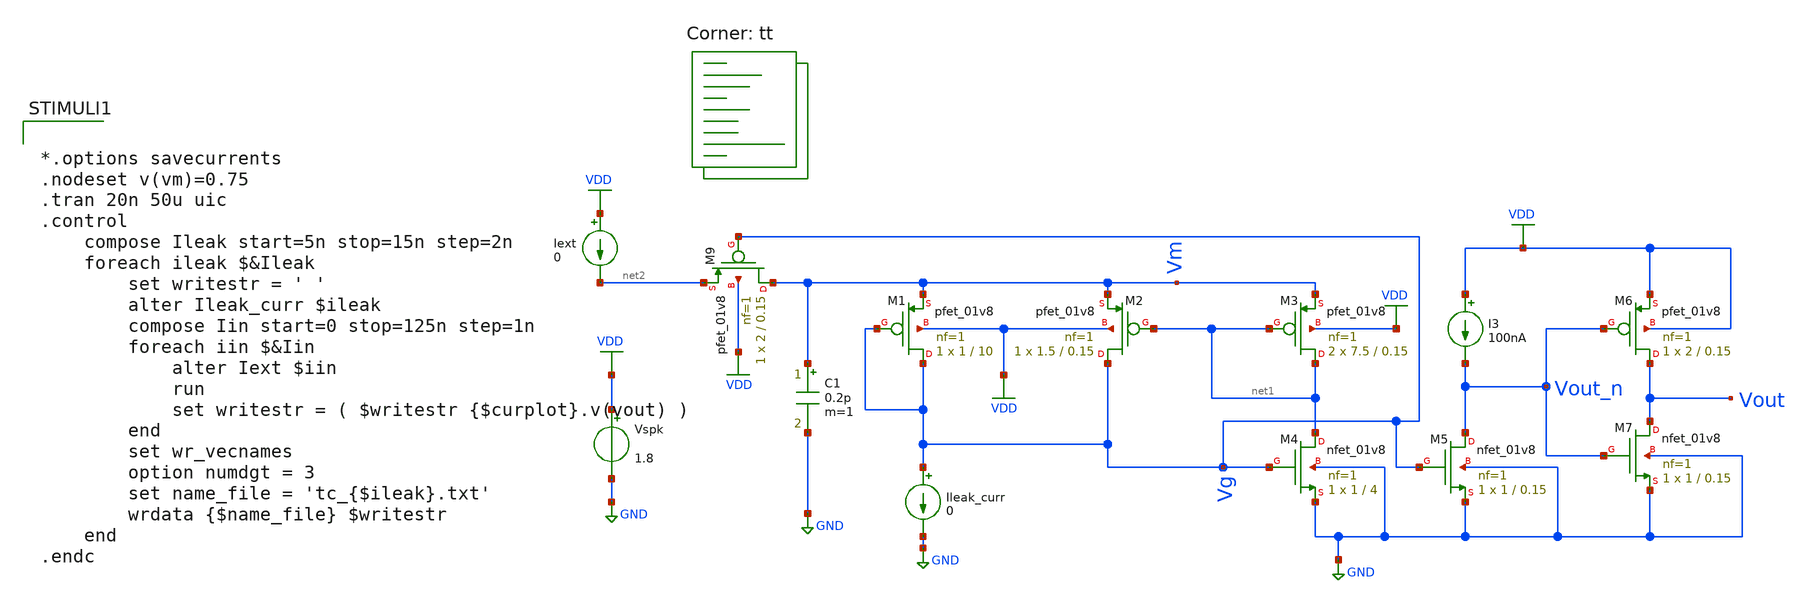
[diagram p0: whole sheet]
** sch_path: Neuron/ultralif/tb_tc_full.sch
**.subckt tb_tc_full
XM1 Vg Vg Vm VDD sky130_fd_pr__pfet_01v8 L=10 W=1 nf=1 ad='int((nf+1)/2) * W/nf * 0.29' as='int((nf+2)/2) * W/nf * 0.29'
+ pd='2*int((nf+1)/2) * (W/nf + 0.29)' ps='2*int((nf+2)/2) * (W/nf + 0.29)' nrd='0.29 / W' nrs='0.29 / W'
+ sa=0 sb=0 sd=0 mult=1 m=1
XM2 Vg net1 Vm VDD sky130_fd_pr__pfet_01v8 L=0.15 W=1.5 nf=1 ad='int((nf+1)/2) * W/nf * 0.29' as='int((nf+2)/2) * W/nf * 0.29'
+ pd='2*int((nf+1)/2) * (W/nf + 0.29)' ps='2*int((nf+2)/2) * (W/nf + 0.29)' nrd='0.29 / W' nrs='0.29 / W'
+ sa=0 sb=0 sd=0 mult=1 m=1
XM3 net1 net1 Vm VDD sky130_fd_pr__pfet_01v8 L=0.15 W=7.5 nf=1 ad='int((nf+1)/2) * W/nf * 0.29' as='int((nf+2)/2) * W/nf * 0.29'
+ pd='2*int((nf+1)/2) * (W/nf + 0.29)' ps='2*int((nf+2)/2) * (W/nf + 0.29)' nrd='0.29 / W' nrs='0.29 / W'
+ sa=0 sb=0 sd=0 mult=2 m=2
XM4 net1 Vg GND GND sky130_fd_pr__nfet_01v8 L=4 W=1 nf=1 ad='int((1 + 1)/2) * 1 / 1 * 0.29' as='int((1 + 2)/2) * 1 / 1 * 0.29'
+ pd='2*int((1 + 1)/2) * (1 / 1 + 0.29)' ps='2*int((1 + 2)/2) * (1 / 1 + 0.29)' nrd='0.29 / 1 ' nrs='0.29 / 1 '
+ sa=0 sb=0 sd=0 mult=1 m=1
XM5 Vout_n Vg GND GND sky130_fd_pr__nfet_01v8 L=0.15 W=1 nf=1 ad='int((1 + 1)/2) * 1 / 1 * 0.29' as='int((1 + 2)/2) * 1 / 1 * 0.29'
+ pd='2*int((1 + 1)/2) * (1 / 1 + 0.29)' ps='2*int((1 + 2)/2) * (1 / 1 + 0.29)' nrd='0.29 / 1 ' nrs='0.29 / 1 '
+ sa=0 sb=0 sd=0 mult=1 m=1
XM6 Vout Vout_n VDD VDD sky130_fd_pr__pfet_01v8 L=0.15 W=2 nf=1 ad='int((nf+1)/2) * W/nf * 0.29' as='int((nf+2)/2) * W/nf * 0.29'
+ pd='2*int((nf+1)/2) * (W/nf + 0.29)' ps='2*int((nf+2)/2) * (W/nf + 0.29)' nrd='0.29 / W' nrs='0.29 / W'
+ sa=0 sb=0 sd=0 mult=1 m=1
XM7 Vout Vout_n GND GND sky130_fd_pr__nfet_01v8 L=0.15 W=1 nf=1 ad='int((1 + 1)/2) * 1 / 1 * 0.29' as='int((1 + 2)/2) * 1 / 1 * 0.29'
+ pd='2*int((1 + 1)/2) * (1 / 1 + 0.29)' ps='2*int((1 + 2)/2) * (1 / 1 + 0.29)' nrd='0.29 / 1 ' nrs='0.29 / 1 '
+ sa=0 sb=0 sd=0 mult=1 m=1
Ileak_curr Vg GND 0
Vspk VDD GND 1.8
C1 Vm GND 0.2p m=1
Iext VDD net2 0
I3 VDD Vout_n 100nA
XM9 Vm Vg net2 VDD sky130_fd_pr__pfet_01v8 L=0.15 W=2 nf=1 ad='int((nf+1)/2) * W/nf * 0.29' as='int((nf+2)/2) * W/nf * 0.29'
+ pd='2*int((nf+1)/2) * (W/nf + 0.29)' ps='2*int((nf+2)/2) * (W/nf + 0.29)' nrd='0.29 / W' nrs='0.29 / W'
+ sa=0 sb=0 sd=0 mult=1 m=1
**** begin user architecture code
.lib $::SKYWATER_MODELS/sky130.lib.spice tt
**** end user architecture code
**.ends
.GLOBAL GND
.GLOBAL VDD
**** begin user architecture code


*.options savecurrents
.nodeset v(vm)=0.75
.tran 20n 50u uic
.control
	compose Ileak start=5n stop=15n step=2n
	foreach ileak $&Ileak
		set writestr = ' '
		alter Ileak_curr $ileak
		compose Iin start=0 stop=125n step=1n
		foreach iin $&Iin
			alter Iext $iin
			run
			set writestr = ( $writestr {$curplot}.v(vout) )
		end
		set wr_vecnames
		option numdgt = 3
		set name_file = 'tc_{$ileak}.txt'
		wrdata {$name_file} $writestr
	end
.endc


**** end user architecture code
.end
